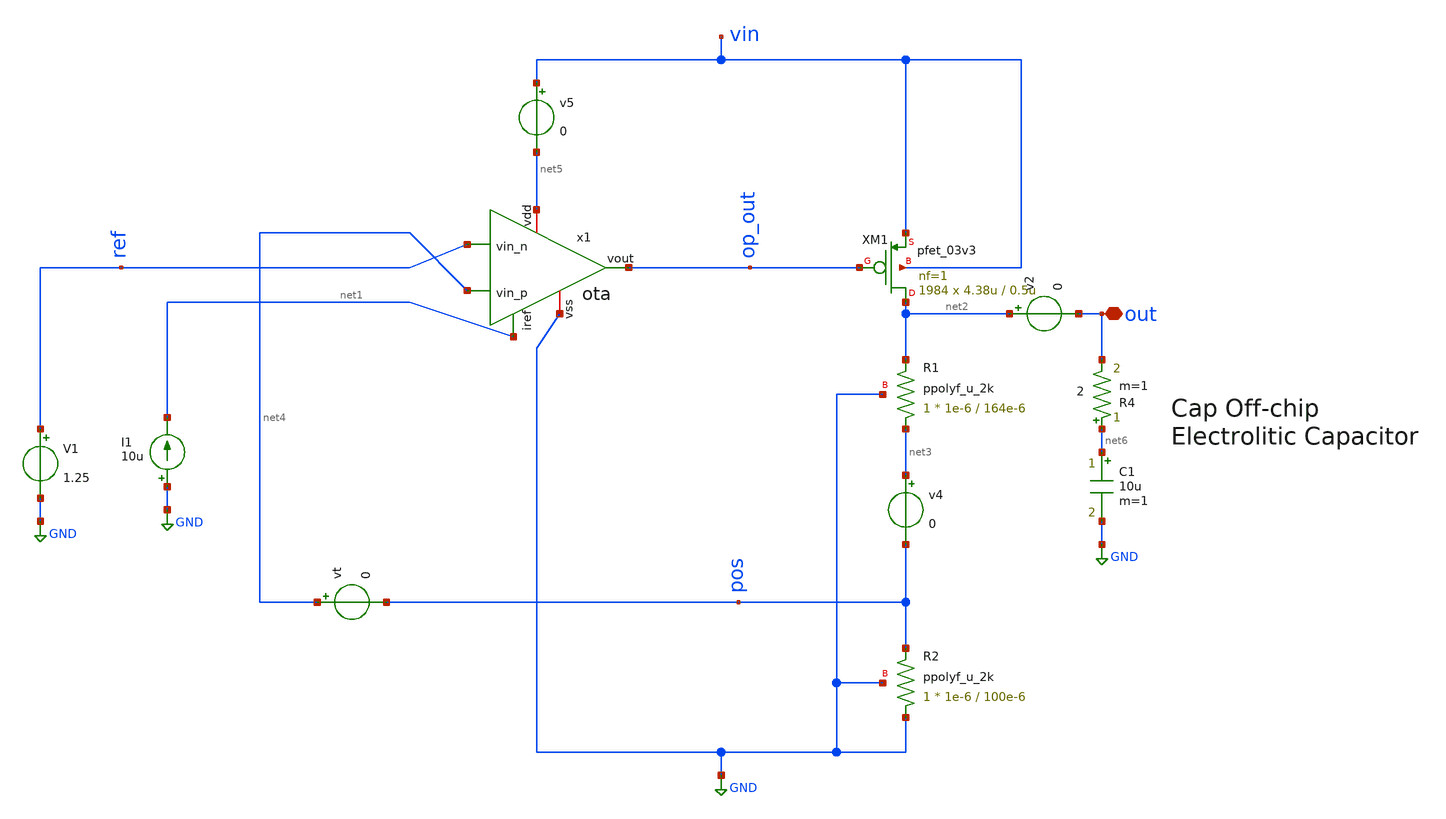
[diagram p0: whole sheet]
** sch_path: LDO/xschem/ldo/test/quisient_current.sch

.include $env(PDK_ROOT)/$env(PDK)/libs.tech/ngspice/design.ngspice
.lib $env(PDK_ROOT)/$env(PDK)/libs.tech/ngspice/sm141064.ngspice typical
.lib $env(PDK_ROOT)/$env(PDK)/libs.tech/ngspice/sm141064.ngspice res_typical

.lib $env(PDK_ROOT)/$env(PDK)/libs.tech/ngspice/sm141064.ngspice cap_mim
.lib $env(PDK_ROOT)/$env(PDK)/libs.tech/ngspice/sm141064.ngspice mimcap_typical


**.subckt quisient_current out
*.iopin out
I1 GND net1 10u
V1 ref GND 1.25
XM1 net2 op_out vin vin pfet_03v3 L=0.5u W=4.38u nf=1 ad='int((nf+1)/2) * W/nf * 0.18u' as='int((nf+2)/2) * W/nf * 0.18u'
+ pd='2*int((nf+1)/2) * (W/nf + 0.18u)' ps='2*int((nf+2)/2) * (W/nf + 0.18u)' nrd='0.18u / W' nrs='0.18u / W'
+ sa=0 sb=0 sd=0 m=1984
XR1 net3 net2 GND ppolyf_u_2k r_width=1e-6 r_length=164e-6 m=1
XR2 GND pos GND ppolyf_u_2k r_width=1e-6 r_length=100e-6 m=1
v4 net3 pos 0
vt net4 pos 0
v2 net2 out 0
v5 vin net5 0
x1 net5 net1 ref net4 op_out GND ota
C1 net6 GND 10u m=1
R4 net6 out 2 m=1
**** begin user architecture code


.param R=33
R10 out 0 {R}
*IL out 0 PWL(0 0.1m 10u 0.1m 20u 10m 30u 10m)

IL out 0 DC 10m

.param iref = 10u
.param vdd  = 5
.param vss  = 0.0
.param vcm  = 1.25
.param vac  = 60m
.param w857 = 5u
.param l857 = 1u
.param m857 = 1
.param wpar = 10u
.param lpar = 1u
.param mpar = 1
.param w34  = 10u
.param l34  = 1u
.param m34  = 1
.param w6   = 100u
.param l6   = 1u
.param m6   = 1

.param m5   = 1
.param m7   = 5


Vs vin 0 5

.nodeset v(out)=0
.nodeset v(x1.pos)=0

*TRANSIENT
.control
save all
tran 1ns 100us
let gds = @x1.xm2.m0[gds]
print ic
plot gds
*plot v(out) v(ref) v(pos) v(vin)
plot i(v5) i(v2)
*plot v(op_out)
*plot v(op_out)
*plot v(out)
*plot i(out)
*plot i(v3)*v(vin)
meas tran il FIND i(v2) WHEN time=90u
meas tran iq FIND i(v5) WHEN time=90u
.endc


**** end user architecture code
**.ends
.GLOBAL GND
.end
